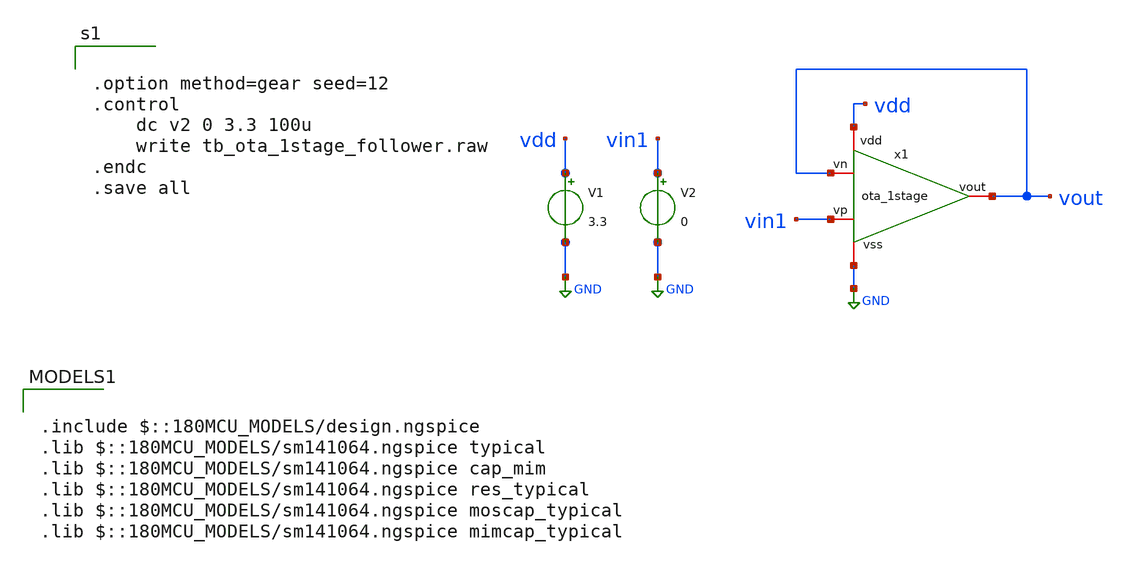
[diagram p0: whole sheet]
** sch_path: designs/libs/core_LIF_comp/tb_ota_1stage/tb_ota_1stage_follower.sch
**.subckt tb_ota_1stage_follower
V1 vdd GND 3.3
V2 vin1 GND 0
x1 vdd vout vin1 vout GND ota_1stage
**** begin user architecture code


.option method=gear seed=12
.control
    dc v2 0 3.3 100u
    write tb_ota_1stage_follower.raw
.endc
.save all



.include $::180MCU_MODELS/design.ngspice
.lib $::180MCU_MODELS/sm141064.ngspice typical
.lib $::180MCU_MODELS/sm141064.ngspice cap_mim
.lib $::180MCU_MODELS/sm141064.ngspice res_typical
.lib $::180MCU_MODELS/sm141064.ngspice moscap_typical
.lib $::180MCU_MODELS/sm141064.ngspice mimcap_typical

**** end user architecture code
**.ends

* expanding   symbol:  designs/libs/core_LIF_comp/core_ota_1stage/ota_1stage.sym # of pins=5
** sym_path: designs/libs/core_LIF_comp/core_ota_1stage/ota_1stage.sym
** sch_path: designs/libs/core_LIF_comp/core_ota_1stage/ota_1stage.sch
.subckt ota_1stage vdd vout vp vn vss
*.iopin vdd
*.iopin vss
*.iopin vp
*.iopin vn
*.iopin vout
XM1 net1 net1 vdd vdd pfet_03v3 L=0.28u W=0.84u nf=1 ad='int((nf+1)/2) * W/nf * 0.18u' as='int((nf+2)/2) * W/nf * 0.18u'
+ pd='2*int((nf+1)/2) * (W/nf + 0.18u)' ps='2*int((nf+2)/2) * (W/nf + 0.18u)' nrd='0.18u / W' nrs='0.18u / W'
+ sa=0 sb=0 sd=0 m=1
XM2 net1 vp net2 vss nfet_03v3 L=0.28u W=3.08u nf=1 ad='int((nf+1)/2) * W/nf * 0.18u' as='int((nf+2)/2) * W/nf * 0.18u'
+ pd='2*int((nf+1)/2) * (W/nf + 0.18u)' ps='2*int((nf+2)/2) * (W/nf + 0.18u)' nrd='0.18u / W' nrs='0.18u / W'
+ sa=0 sb=0 sd=0 m=1
XM4 vout net1 vdd vdd pfet_03v3 L=0.28u W=0.84u nf=1 ad='int((nf+1)/2) * W/nf * 0.18u' as='int((nf+2)/2) * W/nf * 0.18u'
+ pd='2*int((nf+1)/2) * (W/nf + 0.18u)' ps='2*int((nf+2)/2) * (W/nf + 0.18u)' nrd='0.18u / W' nrs='0.18u / W'
+ sa=0 sb=0 sd=0 m=1
XM3 vout vn net2 vss nfet_03v3 L=0.28u W=3.08u nf=1 ad='int((nf+1)/2) * W/nf * 0.18u' as='int((nf+2)/2) * W/nf * 0.18u'
+ pd='2*int((nf+1)/2) * (W/nf + 0.18u)' ps='2*int((nf+2)/2) * (W/nf + 0.18u)' nrd='0.18u / W' nrs='0.18u / W'
+ sa=0 sb=0 sd=0 m=1
XM5 net2 net3 vss vss nfet_03v3 L=0.28u W=0.84u nf=1 ad='int((nf+1)/2) * W/nf * 0.18u' as='int((nf+2)/2) * W/nf * 0.18u'
+ pd='2*int((nf+1)/2) * (W/nf + 0.18u)' ps='2*int((nf+2)/2) * (W/nf + 0.18u)' nrd='0.18u / W' nrs='0.18u / W'
+ sa=0 sb=0 sd=0 m=1
XM6 net3 net3 vss vss nfet_03v3 L=0.28u W=0.84u nf=1 ad='int((nf+1)/2) * W/nf * 0.18u' as='int((nf+2)/2) * W/nf * 0.18u'
+ pd='2*int((nf+1)/2) * (W/nf + 0.18u)' ps='2*int((nf+2)/2) * (W/nf + 0.18u)' nrd='0.18u / W' nrs='0.18u / W'
+ sa=0 sb=0 sd=0 m=1
XM7 vdd vdd net3 vss nfet_03v3 L=8.54u W=0.28u nf=1 ad='int((nf+1)/2) * W/nf * 0.18u' as='int((nf+2)/2) * W/nf * 0.18u'
+ pd='2*int((nf+1)/2) * (W/nf + 0.18u)' ps='2*int((nf+2)/2) * (W/nf + 0.18u)' nrd='0.18u / W' nrs='0.18u / W'
+ sa=0 sb=0 sd=0 m=1
.ends

.GLOBAL GND
.end
